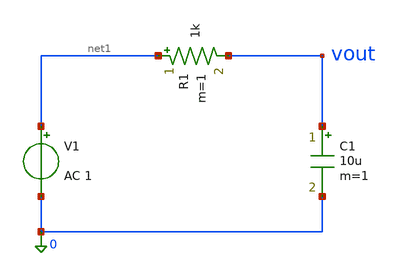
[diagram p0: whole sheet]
** sch_path: RC Low Pass Filter/Schematic/schematic.sch
**.subckt schematic
R1 net1 vout 1k m=1
C1 vout 0 10u m=1
V1 net1 0 AC 1
**** begin user architecture code


.control
  set color1=black
  ac dec 20 1 100k
  run
  let vdb = db(vout)
  let dc_gain = vdb[0]
  meas ac f_3db when vdb=dc_gain-3
  plot db(vout)
.endc


**** end user architecture code
**.ends
.end
